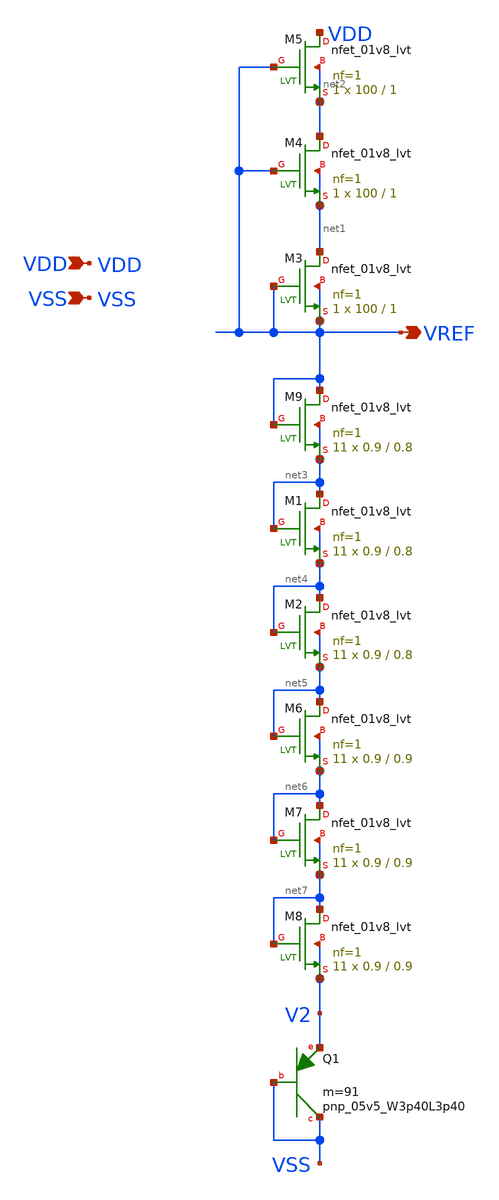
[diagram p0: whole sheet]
** sch_path: design/LELO_SVOD_SKY130A/LELO_SVOD_VTREF.sch
**.subckt LELO_SVOD_VTREF VDD VSS VREF
*.ipin VDD
*.ipin VSS
*.opin VREF
XQ1 VSS VSS V2 sky130_fd_pr__pnp_05v5_W3p40L3p40 m=91
XM3 net1 VREF VREF VREF sky130_fd_pr__nfet_01v8_lvt L=1 W=100 nf=1 ad='int((1 + 1)/2) * 100 / 1 * 0.29'
+ as='int((1 + 2)/2) * 100 / 1 * 0.29' pd='2*int((1 + 1)/2) * (100 / 1 + 0.29)' ps='2*int((1 + 2)/2) * (100 / 1 + 0.29)'
+ nrd='0.29 / 100 ' nrs='0.29 / 100 ' sa=0 sb=0 sd=0 mult=1 m=1
XM4 net2 VREF net1 net1 sky130_fd_pr__nfet_01v8_lvt L=1 W=100 nf=1 ad='int((1 + 1)/2) * 100 / 1 * 0.29'
+ as='int((1 + 2)/2) * 100 / 1 * 0.29' pd='2*int((1 + 1)/2) * (100 / 1 + 0.29)' ps='2*int((1 + 2)/2) * (100 / 1 + 0.29)'
+ nrd='0.29 / 100 ' nrs='0.29 / 100 ' sa=0 sb=0 sd=0 mult=1 m=1
XM5 VDD VREF net2 net2 sky130_fd_pr__nfet_01v8_lvt L=1 W=100 nf=1 ad='int((1 + 1)/2) * 100 / 1 * 0.29'
+ as='int((1 + 2)/2) * 100 / 1 * 0.29' pd='2*int((1 + 1)/2) * (100 / 1 + 0.29)' ps='2*int((1 + 2)/2) * (100 / 1 + 0.29)'
+ nrd='0.29 / 100 ' nrs='0.29 / 100 ' sa=0 sb=0 sd=0 mult=1 m=1
XM9 VREF VREF net3 net3 sky130_fd_pr__nfet_01v8_lvt L=0.8 W=0.9 nf=1 ad='int((1 + 1)/2) * 0.9 / 1 * 0.29'
+ as='int((1 + 2)/2) * 0.9 / 1 * 0.29' pd='2*int((1 + 1)/2) * (0.9 / 1 + 0.29)' ps='2*int((1 + 2)/2) * (0.9 / 1 + 0.29)'
+ nrd='0.29 / 0.9 ' nrs='0.29 / 0.9 ' sa=0 sb=0 sd=0 mult=11 m=11
XM1 net3 net3 net4 net4 sky130_fd_pr__nfet_01v8_lvt L=0.8 W=0.9 nf=1 ad='int((1 + 1)/2) * 0.9 / 1 * 0.29'
+ as='int((1 + 2)/2) * 0.9 / 1 * 0.29' pd='2*int((1 + 1)/2) * (0.9 / 1 + 0.29)' ps='2*int((1 + 2)/2) * (0.9 / 1 + 0.29)'
+ nrd='0.29 / 0.9 ' nrs='0.29 / 0.9 ' sa=0 sb=0 sd=0 mult=11 m=11
XM2 net4 net4 net5 net5 sky130_fd_pr__nfet_01v8_lvt L=0.8 W=0.9 nf=1 ad='int((1 + 1)/2) * 0.9 / 1 * 0.29'
+ as='int((1 + 2)/2) * 0.9 / 1 * 0.29' pd='2*int((1 + 1)/2) * (0.9 / 1 + 0.29)' ps='2*int((1 + 2)/2) * (0.9 / 1 + 0.29)'
+ nrd='0.29 / 0.9 ' nrs='0.29 / 0.9 ' sa=0 sb=0 sd=0 mult=11 m=11
XM6 net5 net5 net6 net6 sky130_fd_pr__nfet_01v8_lvt L=0.9 W=0.9 nf=1 ad='int((1 + 1)/2) * 0.9 / 1 * 0.29'
+ as='int((1 + 2)/2) * 0.9 / 1 * 0.29' pd='2*int((1 + 1)/2) * (0.9 / 1 + 0.29)' ps='2*int((1 + 2)/2) * (0.9 / 1 + 0.29)'
+ nrd='0.29 / 0.9 ' nrs='0.29 / 0.9 ' sa=0 sb=0 sd=0 mult=11 m=11
XM7 net6 net6 net7 net7 sky130_fd_pr__nfet_01v8_lvt L=0.9 W=0.9 nf=1 ad='int((1 + 1)/2) * 0.9 / 1 * 0.29'
+ as='int((1 + 2)/2) * 0.9 / 1 * 0.29' pd='2*int((1 + 1)/2) * (0.9 / 1 + 0.29)' ps='2*int((1 + 2)/2) * (0.9 / 1 + 0.29)'
+ nrd='0.29 / 0.9 ' nrs='0.29 / 0.9 ' sa=0 sb=0 sd=0 mult=11 m=11
XM8 net7 net7 V2 V2 sky130_fd_pr__nfet_01v8_lvt L=0.9 W=0.9 nf=1 ad='int((1 + 1)/2) * 0.9 / 1 * 0.29'
+ as='int((1 + 2)/2) * 0.9 / 1 * 0.29' pd='2*int((1 + 1)/2) * (0.9 / 1 + 0.29)' ps='2*int((1 + 2)/2) * (0.9 / 1 + 0.29)'
+ nrd='0.29 / 0.9 ' nrs='0.29 / 0.9 ' sa=0 sb=0 sd=0 mult=11 m=11
**.ends
.end
